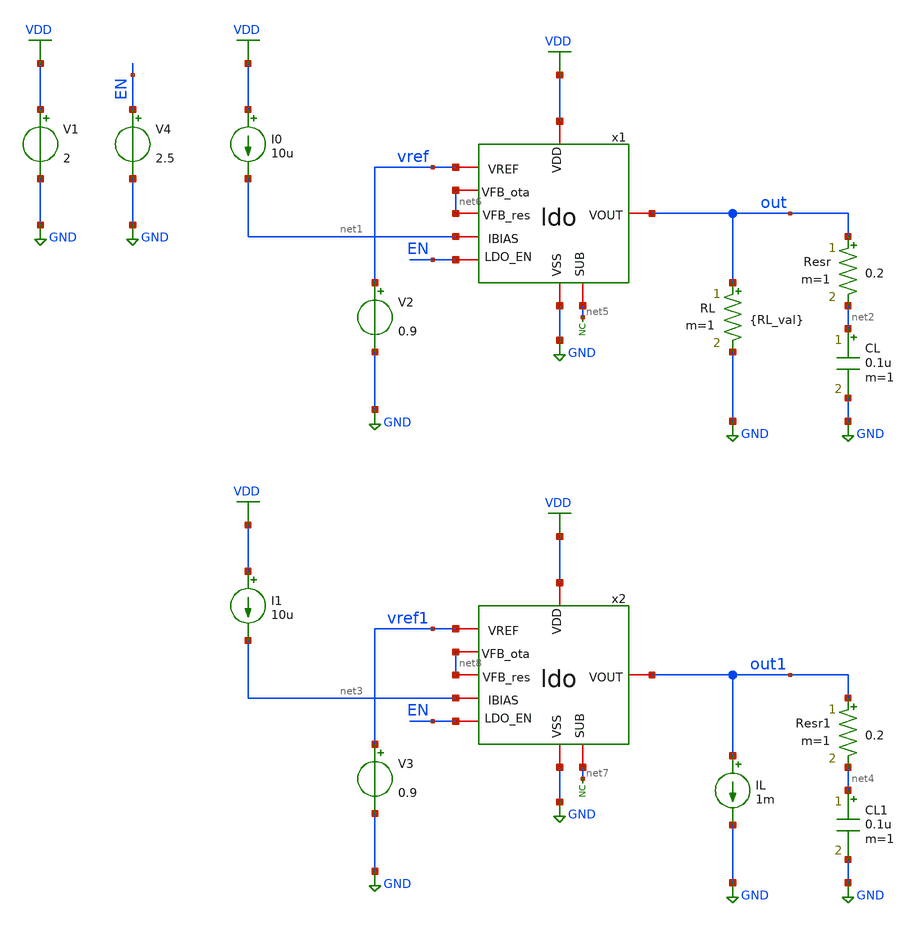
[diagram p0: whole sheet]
** sch_path: designs/libs/tb_ldo/tb_ldo_dc/tb_ldo_dc.sch
**.subckt tb_ldo_dc
RL out GND {RL_val} m=1
V1 VDD GND 2
V2 vref GND 0.9
I0 VDD net1 10u
CL net2 GND 0.1u m=1
Resr out net2 0.2 m=1
IL out1 GND 1m
V3 vref1 GND 0.9
I1 VDD net3 10u
CL1 net4 GND 0.1u m=1
Resr1 out1 net4 0.2 m=1
* noconn #net5
* noconn #net7
x1 VDD vref out net1 net5 GND EN net6 net6 ldo
x2 VDD vref1 out1 net3 net7 GND EN net8 net8 ldo
V4 EN GND 2.5
**** begin user architecture code



.control
save all

run
set color0 = white

** Define param
.param RL_val = 1.8k

** Max load current simulation
dc IL 0 5m 0.01m

**Measurements
meas dc ILOAD_max WHEN v(out1)=1.8
print ILOAD_max

** Plots
setplot dc1
let vout=v(out1)
plot vout

write tb_ldo_dc1.raw

** Dropout voltage simulation
alter RL = {RL_val}
dc V1 0 5 0.01

** Measurements
meas dc Vdd_min FIND v(vdd) WHEN v(out)=1.8 RISE=1
let Vdropout=Vdd_min-1.8
print Vdropout

** Plots
setplot dc2
let vout=v(out)
let vin=v(vdd)
plot vout vin

write tb_ldo_dc2.raw

** Line regulation simulation
alter RL = {RL_val}
dc V1 2 5 0.01

** Measurements
meas dc Vout_max MAX v(out)
meas dc Vout_min MIN v(out)
let DeltaVdd=5-2
let DeltaVout=Vout_max-Vout_min
let Line_reg=DeltaVout/DeltaVdd
print Line_reg

** Plots
setplot dc3
let vout=v(out)
plot vout

write tb_ldo_dc3.raw

** Load regulation simulation
dc IL 0 1m 0.01m

** Measurements
meas dc Vout_max MAX v(out1)
meas dc Vout_min MIN v(out1)
let DeltaVout = Vout_max-Vout_min
let DeltaIload = 0-1m
let Load_reg = abs(DeltaVout/DeltaIload)
let Load_reg_por = (DeltaVout/1.8)*100
print Load_reg
print Load_reg_por

** Plots
setplot dc4
let vout=v(out1)
plot vout

write tb_ldo_dc4.raw

.endc
* ngspice commands




.include $::180MCU_MODELS/design.ngspice
.lib $::180MCU_MODELS/sm141064.ngspice typical
.lib $::180MCU_MODELS/sm141064.ngspice cap_mim
.lib $::180MCU_MODELS/sm141064.ngspice moscap_typical
.lib $::180MCU_MODELS/sm141064.ngspice mimcap_typical
.lib $::180MCU_MODELS/sm141064.ngspice res_typical
* .lib $::180MCU_MODELS/sm141064.ngspice res_statistical
* ngspice commands

**** end user architecture code
**.ends

* expanding   symbol:  libs/core_ldo/ldo/ldo.sym # of pins=9
** sym_path: designs/libs/core_ldo/ldo/ldo.sym
** sch_path: designs/libs/core_ldo/ldo/ldo.sch
.subckt ldo VDD VREF VOUT IBIAS SUB VSS LDO_EN VFB_ota VFB_res
*.iopin VDD
*.iopin VSS
*.iopin VOUT
*.iopin VREF
*.iopin IBIAS
*.ipin LDO_EN
*.iopin VFB_ota
*.iopin VFB_res
*.iopin SUB
XMpass VOUT Vota VDD VDD pfet_05v0 L=0.50u W=50.00u nf=1 ad='int((nf+1)/2) * W/nf * 0.18u' as='int((nf+2)/2) * W/nf * 0.18u'
+ pd='2*int((nf+1)/2) * (W/nf + 0.18u)' ps='2*int((nf+2)/2) * (W/nf + 0.18u)' nrd='0.18u / W' nrs='0.18u / W'
+ sa=0 sb=0 sd=0 m=10
XR1[9] Vr_fb1[9] VOUT VDD ppolyf_u_1k r_width=1e-6 r_length=5e-6 m=1
XR1[8] Vr_fb1[8] Vr_fb1[9] VDD ppolyf_u_1k r_width=1e-6 r_length=5e-6 m=1
XR1[7] Vr_fb1[7] Vr_fb1[8] VDD ppolyf_u_1k r_width=1e-6 r_length=5e-6 m=1
XR1[6] Vr_fb1[6] Vr_fb1[7] VDD ppolyf_u_1k r_width=1e-6 r_length=5e-6 m=1
XR1[5] Vr_fb1[5] Vr_fb1[6] VDD ppolyf_u_1k r_width=1e-6 r_length=5e-6 m=1
XR1[4] Vr_fb1[4] Vr_fb1[5] VDD ppolyf_u_1k r_width=1e-6 r_length=5e-6 m=1
XR1[3] Vr_fb1[3] Vr_fb1[4] VDD ppolyf_u_1k r_width=1e-6 r_length=5e-6 m=1
XR1[2] Vr_fb1[2] Vr_fb1[3] VDD ppolyf_u_1k r_width=1e-6 r_length=5e-6 m=1
XR1[1] Vr_fb1[1] Vr_fb1[2] VDD ppolyf_u_1k r_width=1e-6 r_length=5e-6 m=1
XR1[0] VFB_res Vr_fb1[1] VDD ppolyf_u_1k r_width=1e-6 r_length=5e-6 m=1
XR2[9] Vr_fb2[9] VFB_res VDD ppolyf_u_1k r_width=1e-6 r_length=5e-6 m=1
XR2[8] Vr_fb2[8] Vr_fb2[9] VDD ppolyf_u_1k r_width=1e-6 r_length=5e-6 m=1
XR2[7] Vr_fb2[7] Vr_fb2[8] VDD ppolyf_u_1k r_width=1e-6 r_length=5e-6 m=1
XR2[6] Vr_fb2[6] Vr_fb2[7] VDD ppolyf_u_1k r_width=1e-6 r_length=5e-6 m=1
XR2[5] Vr_fb2[5] Vr_fb2[6] VDD ppolyf_u_1k r_width=1e-6 r_length=5e-6 m=1
XR2[4] Vr_fb2[4] Vr_fb2[5] VDD ppolyf_u_1k r_width=1e-6 r_length=5e-6 m=1
XR2[3] Vr_fb2[3] Vr_fb2[4] VDD ppolyf_u_1k r_width=1e-6 r_length=5e-6 m=1
XR2[2] Vr_fb2[2] Vr_fb2[3] VDD ppolyf_u_1k r_width=1e-6 r_length=5e-6 m=1
XR2[1] Vr_fb2[1] Vr_fb2[2] VDD ppolyf_u_1k r_width=1e-6 r_length=5e-6 m=1
XR2[0] VSS Vr_fb2[1] VDD ppolyf_u_1k r_width=1e-6 r_length=5e-6 m=1
XRc[29] Vr_mc[29] Vmc VDD ppolyf_u_1k r_width=1e-6 r_length=10e-6 m=1
XRc[28] Vr_mc[28] Vr_mc[29] VDD ppolyf_u_1k r_width=1e-6 r_length=10e-6 m=1
XRc[27] Vr_mc[27] Vr_mc[28] VDD ppolyf_u_1k r_width=1e-6 r_length=10e-6 m=1
XRc[26] Vr_mc[26] Vr_mc[27] VDD ppolyf_u_1k r_width=1e-6 r_length=10e-6 m=1
XRc[25] Vr_mc[25] Vr_mc[26] VDD ppolyf_u_1k r_width=1e-6 r_length=10e-6 m=1
XRc[24] Vr_mc[24] Vr_mc[25] VDD ppolyf_u_1k r_width=1e-6 r_length=10e-6 m=1
XRc[23] Vr_mc[23] Vr_mc[24] VDD ppolyf_u_1k r_width=1e-6 r_length=10e-6 m=1
XRc[22] Vr_mc[22] Vr_mc[23] VDD ppolyf_u_1k r_width=1e-6 r_length=10e-6 m=1
XRc[21] Vr_mc[21] Vr_mc[22] VDD ppolyf_u_1k r_width=1e-6 r_length=10e-6 m=1
XRc[20] Vr_mc[20] Vr_mc[21] VDD ppolyf_u_1k r_width=1e-6 r_length=10e-6 m=1
XRc[19] Vr_mc[19] Vr_mc[20] VDD ppolyf_u_1k r_width=1e-6 r_length=10e-6 m=1
XRc[18] Vr_mc[18] Vr_mc[19] VDD ppolyf_u_1k r_width=1e-6 r_length=10e-6 m=1
XRc[17] Vr_mc[17] Vr_mc[18] VDD ppolyf_u_1k r_width=1e-6 r_length=10e-6 m=1
XRc[16] Vr_mc[16] Vr_mc[17] VDD ppolyf_u_1k r_width=1e-6 r_length=10e-6 m=1
XRc[15] Vr_mc[15] Vr_mc[16] VDD ppolyf_u_1k r_width=1e-6 r_length=10e-6 m=1
XRc[14] Vr_mc[14] Vr_mc[15] VDD ppolyf_u_1k r_width=1e-6 r_length=10e-6 m=1
XRc[13] Vr_mc[13] Vr_mc[14] VDD ppolyf_u_1k r_width=1e-6 r_length=10e-6 m=1
XRc[12] Vr_mc[12] Vr_mc[13] VDD ppolyf_u_1k r_width=1e-6 r_length=10e-6 m=1
XRc[11] Vr_mc[11] Vr_mc[12] VDD ppolyf_u_1k r_width=1e-6 r_length=10e-6 m=1
XRc[10] Vr_mc[10] Vr_mc[11] VDD ppolyf_u_1k r_width=1e-6 r_length=10e-6 m=1
XRc[9] Vr_mc[9] Vr_mc[10] VDD ppolyf_u_1k r_width=1e-6 r_length=10e-6 m=1
XRc[8] Vr_mc[8] Vr_mc[9] VDD ppolyf_u_1k r_width=1e-6 r_length=10e-6 m=1
XRc[7] Vr_mc[7] Vr_mc[8] VDD ppolyf_u_1k r_width=1e-6 r_length=10e-6 m=1
XRc[6] Vr_mc[6] Vr_mc[7] VDD ppolyf_u_1k r_width=1e-6 r_length=10e-6 m=1
XRc[5] Vr_mc[5] Vr_mc[6] VDD ppolyf_u_1k r_width=1e-6 r_length=10e-6 m=1
XRc[4] Vr_mc[4] Vr_mc[5] VDD ppolyf_u_1k r_width=1e-6 r_length=10e-6 m=1
XRc[3] Vr_mc[3] Vr_mc[4] VDD ppolyf_u_1k r_width=1e-6 r_length=10e-6 m=1
XRc[2] Vr_mc[2] Vr_mc[3] VDD ppolyf_u_1k r_width=1e-6 r_length=10e-6 m=1
XRc[1] Vr_mc[1] Vr_mc[2] VDD ppolyf_u_1k r_width=1e-6 r_length=10e-6 m=1
XRc[0] VOUT Vr_mc[1] VDD ppolyf_u_1k r_width=1e-6 r_length=10e-6 m=1
XCc Vota Vmc cap_mim_1f0fF c_width=25e-6 c_length=25e-6 m=4
XRfb_dummy_L[7] VDD VDD VDD ppolyf_u_1k r_width=1e-6 r_length=5e-6 m=1
XRfb_dummy_L[6] VDD VDD VDD ppolyf_u_1k r_width=1e-6 r_length=5e-6 m=1
XRfb_dummy_L[5] VDD VDD VDD ppolyf_u_1k r_width=1e-6 r_length=5e-6 m=1
XRfb_dummy_L[4] VDD VDD VDD ppolyf_u_1k r_width=1e-6 r_length=5e-6 m=1
XRfb_dummy_L[3] VDD VDD VDD ppolyf_u_1k r_width=1e-6 r_length=5e-6 m=1
XRfb_dummy_L[2] VDD VDD VDD ppolyf_u_1k r_width=1e-6 r_length=5e-6 m=1
XRfb_dummy_L[1] VDD VDD VDD ppolyf_u_1k r_width=1e-6 r_length=5e-6 m=1
XRfb_dummy_L[0] VDD VDD VDD ppolyf_u_1k r_width=1e-6 r_length=5e-6 m=1
XRfb_dummy_TB[13] VDD VDD VDD ppolyf_u_1k r_width=1e-6 r_length=5e-6 m=1
XRfb_dummy_TB[12] VDD VDD VDD ppolyf_u_1k r_width=1e-6 r_length=5e-6 m=1
XRfb_dummy_TB[11] VDD VDD VDD ppolyf_u_1k r_width=1e-6 r_length=5e-6 m=1
XRfb_dummy_TB[10] VDD VDD VDD ppolyf_u_1k r_width=1e-6 r_length=5e-6 m=1
XRfb_dummy_TB[9] VDD VDD VDD ppolyf_u_1k r_width=1e-6 r_length=5e-6 m=1
XRfb_dummy_TB[8] VDD VDD VDD ppolyf_u_1k r_width=1e-6 r_length=5e-6 m=1
XRfb_dummy_TB[7] VDD VDD VDD ppolyf_u_1k r_width=1e-6 r_length=5e-6 m=1
XRfb_dummy_TB[6] VDD VDD VDD ppolyf_u_1k r_width=1e-6 r_length=5e-6 m=1
XRfb_dummy_TB[5] VDD VDD VDD ppolyf_u_1k r_width=1e-6 r_length=5e-6 m=1
XRfb_dummy_TB[4] VDD VDD VDD ppolyf_u_1k r_width=1e-6 r_length=5e-6 m=1
XRfb_dummy_TB[3] VDD VDD VDD ppolyf_u_1k r_width=1e-6 r_length=5e-6 m=1
XRfb_dummy_TB[2] VDD VDD VDD ppolyf_u_1k r_width=1e-6 r_length=5e-6 m=1
XRfb_dummy_TB[1] VDD VDD VDD ppolyf_u_1k r_width=1e-6 r_length=5e-6 m=1
XRfb_dummy_TB[0] VDD VDD VDD ppolyf_u_1k r_width=1e-6 r_length=5e-6 m=1
x1 VDD net1 net2 Vota IBIAS VSS OTA
* noconn SUB
x2 VDD LDO_EN ENn VSS biasgen_inverter
x3 VDD ENn ENp VSS biasgen_inverter
XMpenpass Vota ENp VDD VDD pfet_05v0 L=0.5u W=2u nf=1 ad='int((nf+1)/2) * W/nf * 0.18u' as='int((nf+2)/2) * W/nf * 0.18u'
+ pd='2*int((nf+1)/2) * (W/nf + 0.18u)' ps='2*int((nf+2)/2) * (W/nf + 0.18u)' nrd='0.18u / W' nrs='0.18u / W'
+ sa=0 sb=0 sd=0 m=1
.ends


* expanding   symbol:  libs/core_ldo/ldo_OTA/OTA.sym # of pins=6
** sym_path: designs/libs/core_ldo/ldo/OTA.sym
** sch_path: designs/libs/core_ldo/ldo/OTA.sch
.subckt OTA VDD VREF VFB VOTA IBIAS VSS
*.iopin VDD
*.iopin VSS
*.iopin VOTA
*.iopin VREF
*.iopin IBIAS
*.iopin VFB
XM3 net2 net2 VDD VDD pfet_05v0 L=2.00u W=8.00u nf=1 ad='int((nf+1)/2) * W/nf * 0.18u' as='int((nf+2)/2) * W/nf * 0.18u'
+ pd='2*int((nf+1)/2) * (W/nf + 0.18u)' ps='2*int((nf+2)/2) * (W/nf + 0.18u)' nrd='0.18u / W' nrs='0.18u / W'
+ sa=0 sb=0 sd=0 m=1
XM4 net3 net3 VDD VDD pfet_05v0 L=2.00u W=8.00u nf=1 ad='int((nf+1)/2) * W/nf * 0.18u' as='int((nf+2)/2) * W/nf * 0.18u'
+ pd='2*int((nf+1)/2) * (W/nf + 0.18u)' ps='2*int((nf+2)/2) * (W/nf + 0.18u)' nrd='0.18u / W' nrs='0.18u / W'
+ sa=0 sb=0 sd=0 m=1
XM5 net4 net2 VDD VDD pfet_05v0 L=2.00u W=8.00u nf=1 ad='int((nf+1)/2) * W/nf * 0.18u' as='int((nf+2)/2) * W/nf * 0.18u'
+ pd='2*int((nf+1)/2) * (W/nf + 0.18u)' ps='2*int((nf+2)/2) * (W/nf + 0.18u)' nrd='0.18u / W' nrs='0.18u / W'
+ sa=0 sb=0 sd=0 m=1
XM6 VOTA net3 VDD VDD pfet_05v0 L=2.00u W=8.00u nf=1 ad='int((nf+1)/2) * W/nf * 0.18u' as='int((nf+2)/2) * W/nf * 0.18u'
+ pd='2*int((nf+1)/2) * (W/nf + 0.18u)' ps='2*int((nf+2)/2) * (W/nf + 0.18u)' nrd='0.18u / W' nrs='0.18u / W'
+ sa=0 sb=0 sd=0 m=2
XM9 IBIAS IBIAS VSS VSS nfet_05v0 L=2.00u W=4.00u nf=1 ad='int((nf+1)/2) * W/nf * 0.18u' as='int((nf+2)/2) * W/nf * 0.18u'
+ pd='2*int((nf+1)/2) * (W/nf + 0.18u)' ps='2*int((nf+2)/2) * (W/nf + 0.18u)' nrd='0.18u / W' nrs='0.18u / W'
+ sa=0 sb=0 sd=0 m=1
XM10 net1 IBIAS VSS VSS nfet_05v0 L=2.00u W=4.00u nf=1 ad='int((nf+1)/2) * W/nf * 0.18u' as='int((nf+2)/2) * W/nf * 0.18u'
+ pd='2*int((nf+1)/2) * (W/nf + 0.18u)' ps='2*int((nf+2)/2) * (W/nf + 0.18u)' nrd='0.18u / W' nrs='0.18u / W'
+ sa=0 sb=0 sd=0 m=1
XM7 net4 net4 VSS VSS nfet_05v0 L=2.00u W=4.00u nf=1 ad='int((nf+1)/2) * W/nf * 0.18u' as='int((nf+2)/2) * W/nf * 0.18u'
+ pd='2*int((nf+1)/2) * (W/nf + 0.18u)' ps='2*int((nf+2)/2) * (W/nf + 0.18u)' nrd='0.18u / W' nrs='0.18u / W'
+ sa=0 sb=0 sd=0 m=1
XM8 VOTA net4 VSS VSS nfet_05v0 L=2.00u W=4.00u nf=1 ad='int((nf+1)/2) * W/nf * 0.18u' as='int((nf+2)/2) * W/nf * 0.18u'
+ pd='2*int((nf+1)/2) * (W/nf + 0.18u)' ps='2*int((nf+2)/2) * (W/nf + 0.18u)' nrd='0.18u / W' nrs='0.18u / W'
+ sa=0 sb=0 sd=0 m=2
XM1 net2 VREF net1 net1 nfet_05v0 L=0.60u W=40.00u nf=1 ad='int((nf+1)/2) * W/nf * 0.18u' as='int((nf+2)/2) * W/nf * 0.18u'
+ pd='2*int((nf+1)/2) * (W/nf + 0.18u)' ps='2*int((nf+2)/2) * (W/nf + 0.18u)' nrd='0.18u / W' nrs='0.18u / W'
+ sa=0 sb=0 sd=0 m=1
XM2 net3 VFB net1 net1 nfet_05v0 L=0.60u W=40.00u nf=1 ad='int((nf+1)/2) * W/nf * 0.18u' as='int((nf+2)/2) * W/nf * 0.18u'
+ pd='2*int((nf+1)/2) * (W/nf + 0.18u)' ps='2*int((nf+2)/2) * (W/nf + 0.18u)' nrd='0.18u / W' nrs='0.18u / W'
+ sa=0 sb=0 sd=0 m=1
.ends


* expanding   symbol:  libs/core_biasgen/biasgen_inverter/biasgen_inverter.sym # of pins=4
** sym_path: designs/libs/core_biasgen/biasgen_inverter/biasgen_inverter.sym
** sch_path: designs/libs/core_biasgen/biasgen_inverter/biasgen_inverter.sch
.subckt biasgen_inverter VDD IN OUT VSS
*.iopin VDD
*.iopin VSS
*.ipin IN
*.opin OUT
XMINV1 OUT IN VSS VSS nfet_05v0 L=0.60u W=0.50u nf=1 ad='int((nf+1)/2) * W/nf * 0.18u' as='int((nf+2)/2) * W/nf * 0.18u'
+ pd='2*int((nf+1)/2) * (W/nf + 0.18u)' ps='2*int((nf+2)/2) * (W/nf + 0.18u)' nrd='0.18u / W' nrs='0.18u / W'
+ sa=0 sb=0 sd=0 m=1
XMINV2 OUT IN VDD VDD pfet_05v0 L=0.50u W=0.60u nf=1 ad='int((nf+1)/2) * W/nf * 0.18u' as='int((nf+2)/2) * W/nf * 0.18u'
+ pd='2*int((nf+1)/2) * (W/nf + 0.18u)' ps='2*int((nf+2)/2) * (W/nf + 0.18u)' nrd='0.18u / W' nrs='0.18u / W'
+ sa=0 sb=0 sd=0 m=1
.ends

.GLOBAL GND
.GLOBAL VDD
.end
